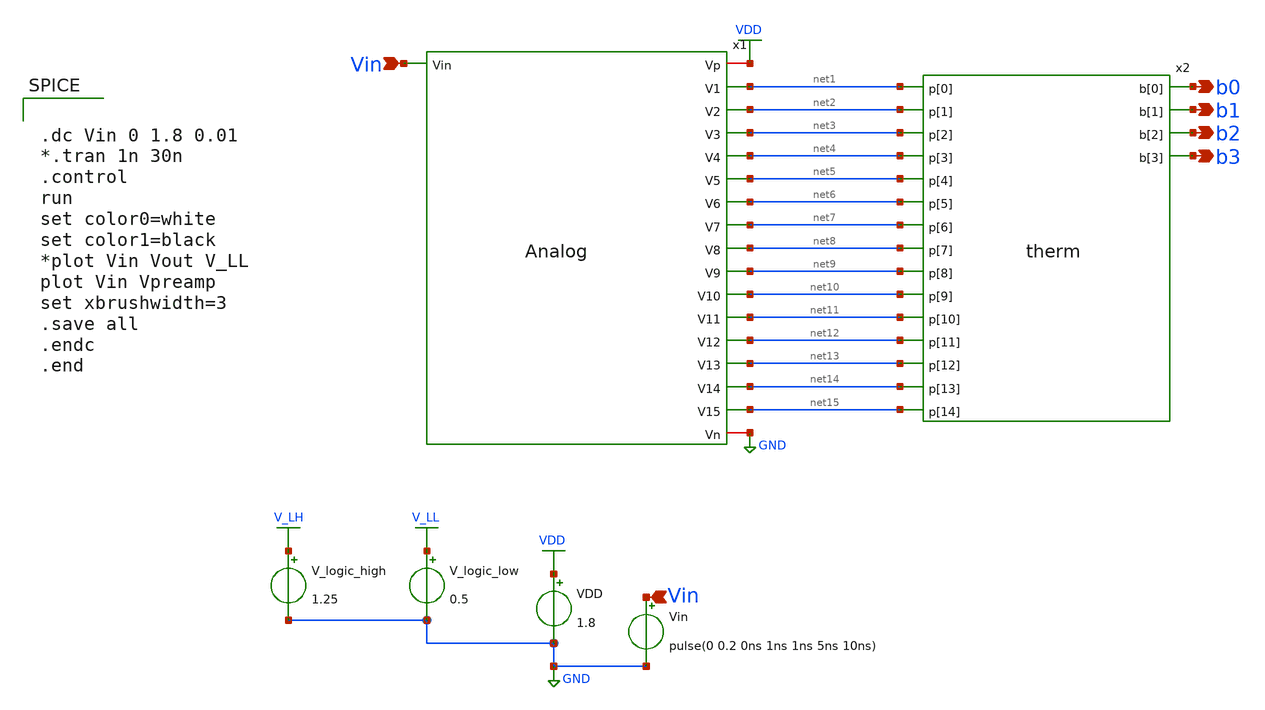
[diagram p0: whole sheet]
** sch_path: xschem/Vth_sch/Pre_layout/analog_therm.sch
**.subckt analog_therm b0 Vin b1 b2 b3 Vin
*.opin b0
*.ipin Vin
*.opin b1
*.opin b2
*.opin b3
*.ipin Vin
VDD VDD GND 1.8
Vin Vin GND pulse(0 0.2 0ns 1ns 1ns 5ns 10ns)
V_logic_high V_LH GND 1.25
V_logic_low V_LL GND 0.5
x1 Vin VDD net1 net2 net3 net4 net5 net6 net7 net8 net9 net10 net11 net12 net13 net14 net15 GND
+ Analog
x2 net1 net2 net3 b0 net4 net5 b1 net6 net7 net8 b2 net9 net10 b3 net11 net12 net13 net14 net15
+ therm
**** begin user architecture code


.lib /usr/local/share/pdk/sky130A/libs.tech/ngspice/sky130.lib.spice tt
.include /usr/local/share/pdk/sky130A/libs.ref/sky130_fd_sc_hd/spice/sky130_fd_sc_hd.spice
.save all





.dc Vin 0 1.8 0.01
*.tran 1n 30n
.control
run
set color0=white
set color1=black
*plot Vin Vout V_LL
plot Vin Vpreamp
set xbrushwidth=3
.save all
.endc
.end


**** end user architecture code
**.ends
.GLOBAL VDD
.GLOBAL GND
.GLOBAL V_LH
.GLOBAL V_LL
.end
